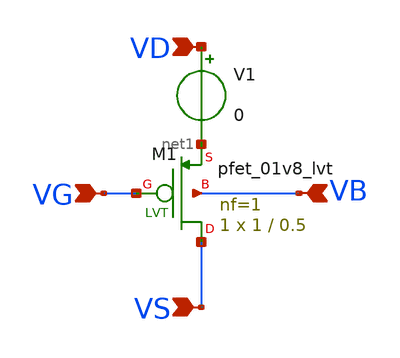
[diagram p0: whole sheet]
** sch_path: design/THESIS_EXP_RO_INVERTER_SKY130A/TB_strength_LVT.sch
**.subckt TB_strength_LVT VD VG VS VB
*.ipin VD
*.ipin VG
*.ipin VS
*.ipin VB
V1 VD net1 0
.save i(v1)
XM1 VS VG net1 VB sky130_fd_pr__pfet_01v8_lvt L=0.5 W=1 nf=1 ad='int((nf+1)/2) * W/nf * 0.29' as='int((nf+2)/2) * W/nf * 0.29'
+ pd='2*int((nf+1)/2) * (W/nf + 0.29)' ps='2*int((nf+2)/2) * (W/nf + 0.29)' nrd='0.29 / W' nrs='0.29 / W'
+ sa=0 sb=0 sd=0 mult=1 m=1
**.ends
.end
